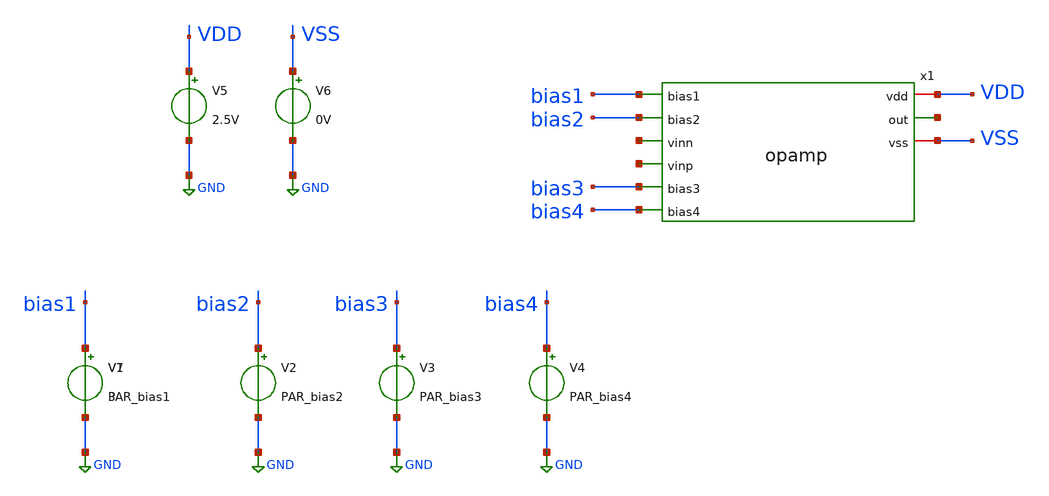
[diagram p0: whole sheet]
** sch_path: activities/opamp2AKAM/testBenchOpamp.sch
**.subckt testBenchOpamp
V1 bias1 GND PAR_bias1
V2 bias2 GND PAR_bias2
V3 bias3 GND PAR_bias3
V4 bias4 GND PAR_bias4
V5 VDD GND 2.5V
V6 VSS GND 0V
V7 bias1 GND 3
x1 VDD bias1 bias2 net1 net2 net3 bias3 bias4 VSS opamp
**.ends
.GLOBAL GND
.end
